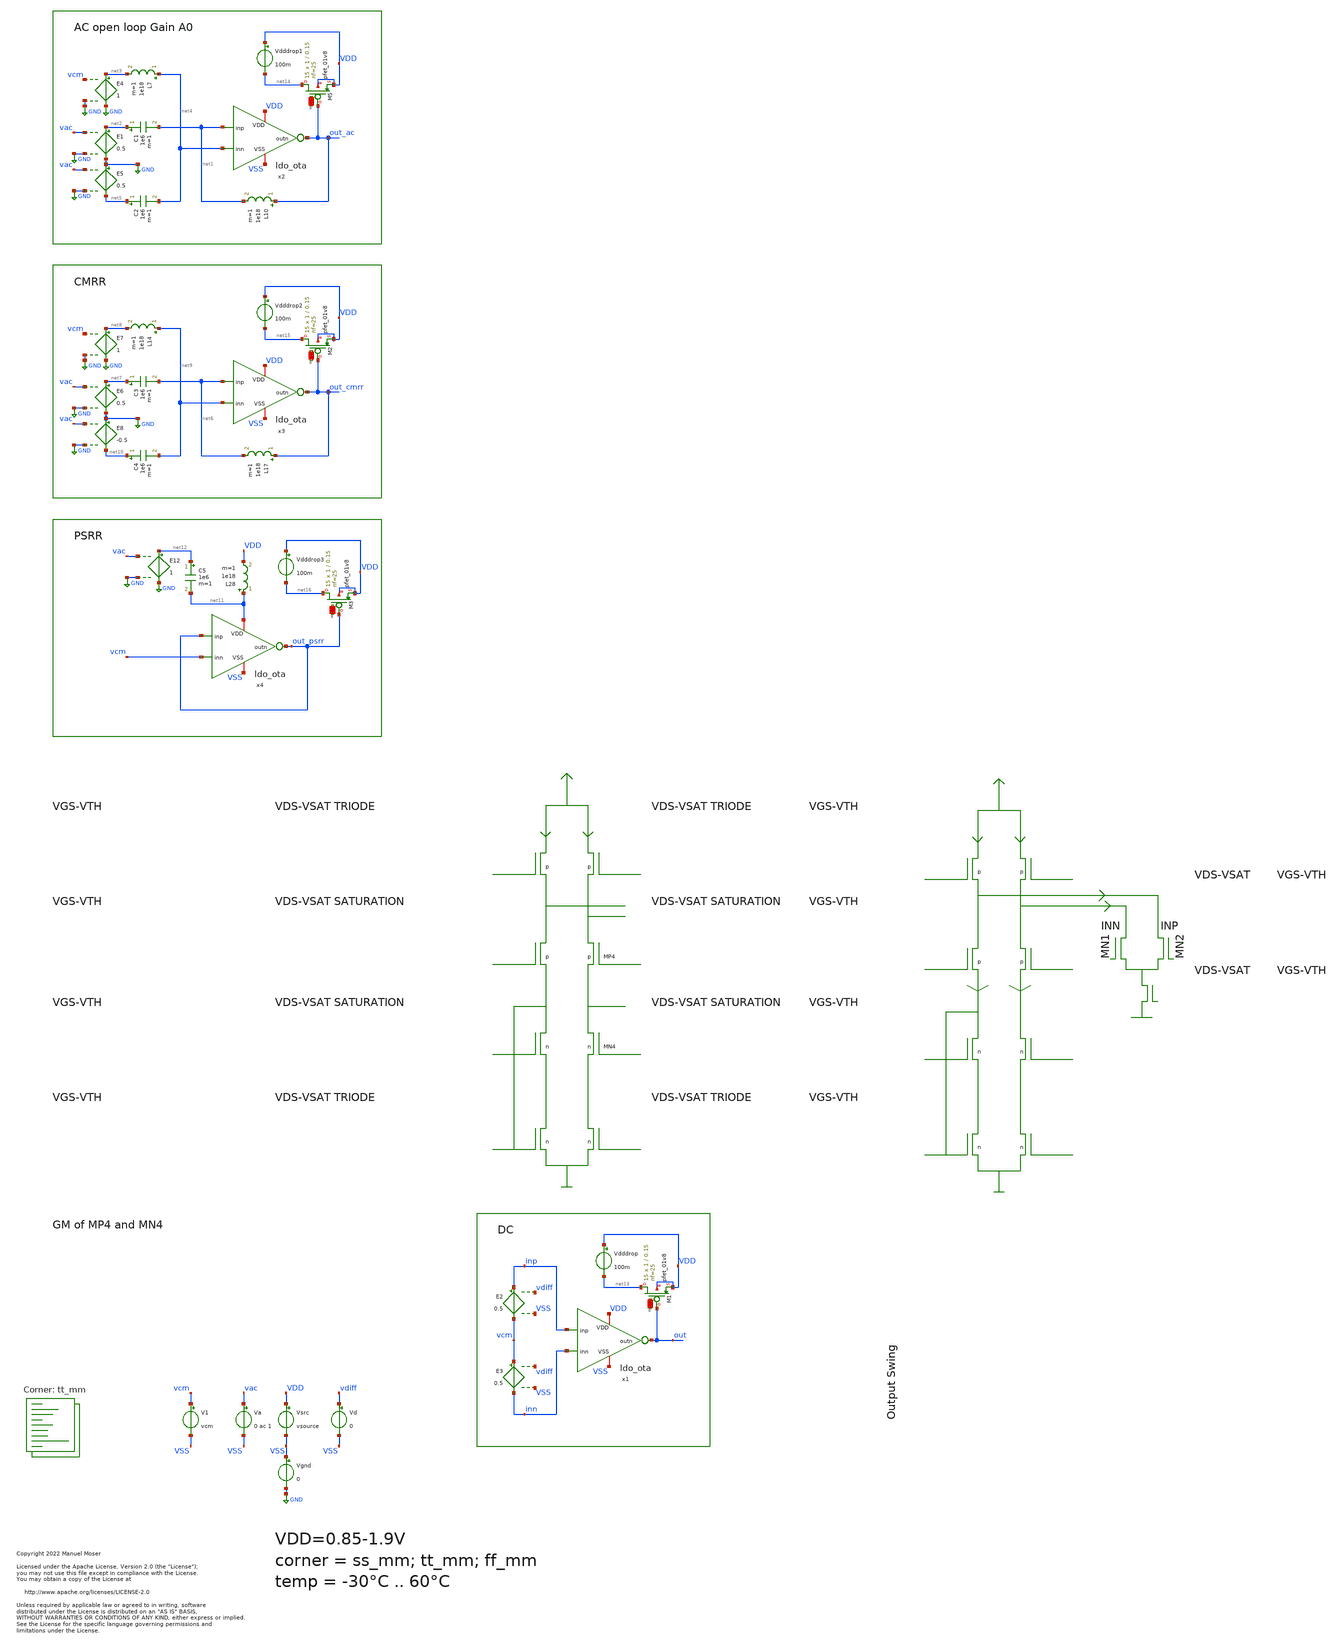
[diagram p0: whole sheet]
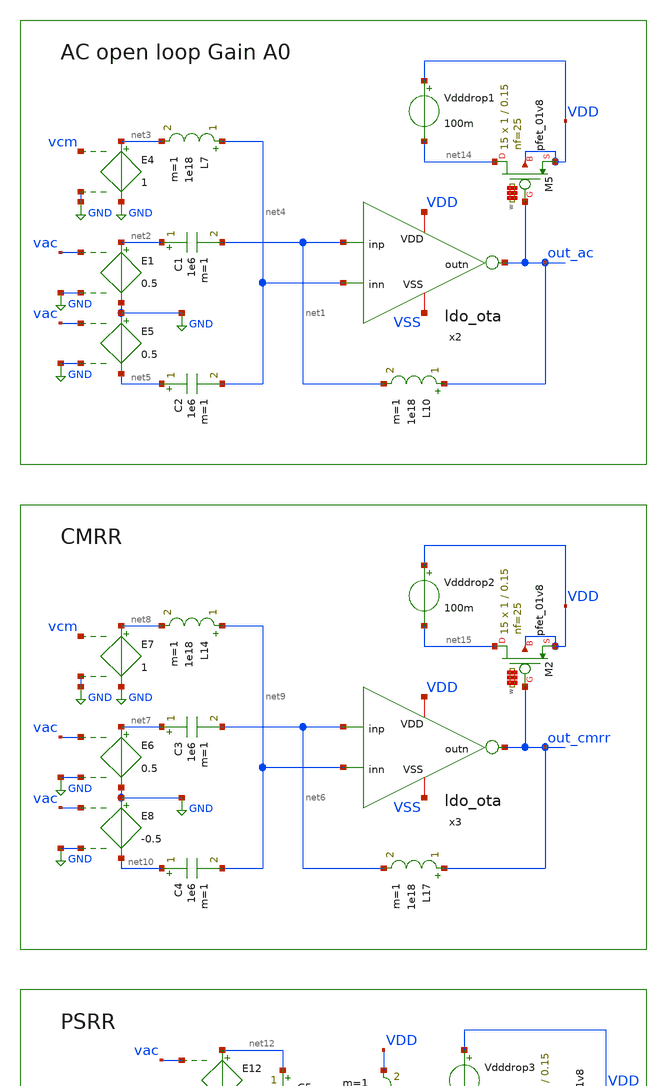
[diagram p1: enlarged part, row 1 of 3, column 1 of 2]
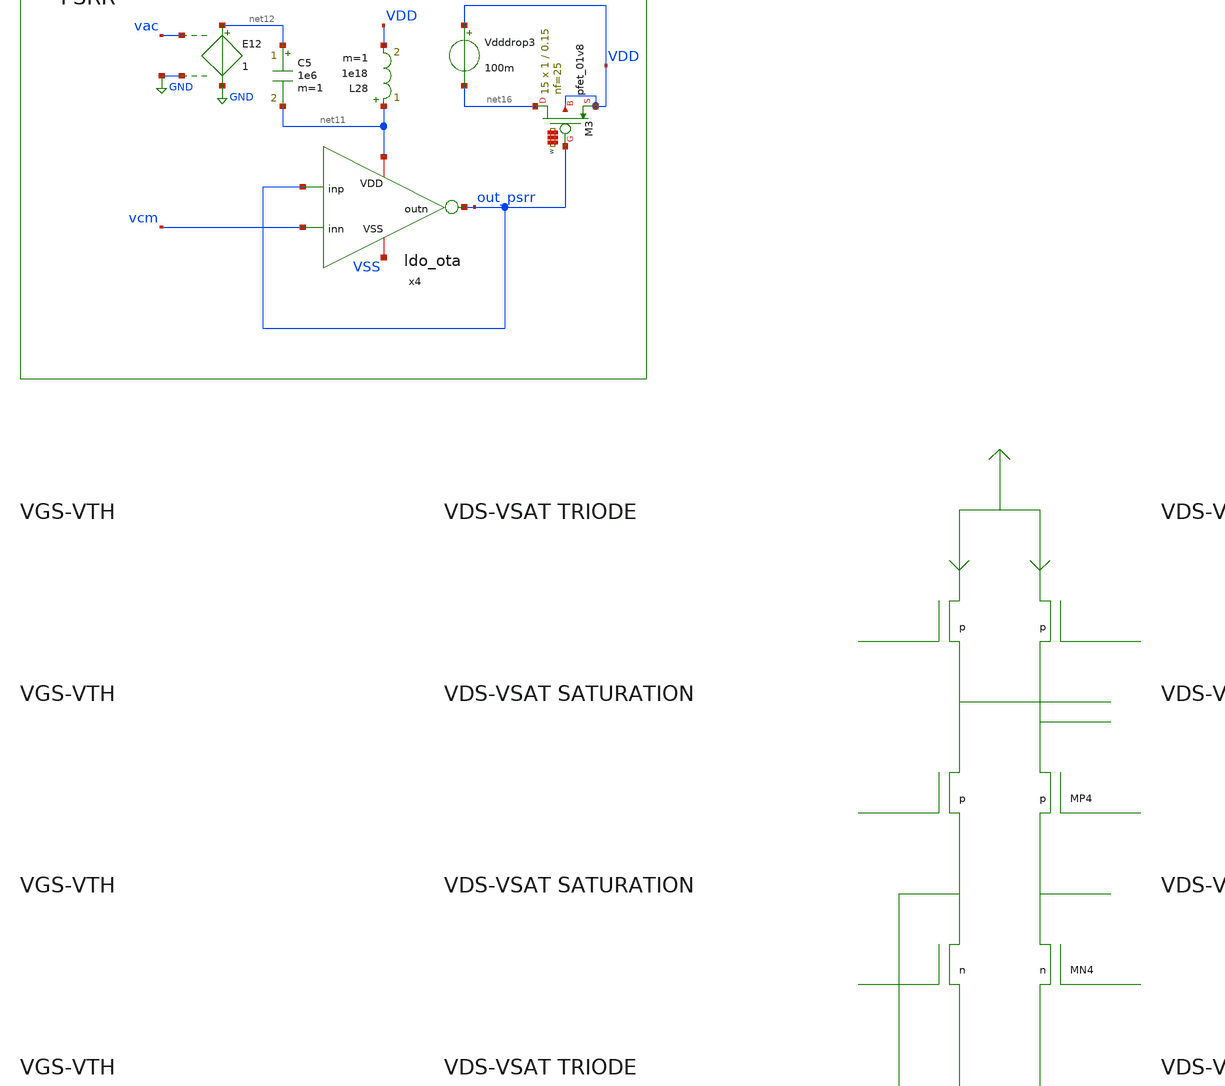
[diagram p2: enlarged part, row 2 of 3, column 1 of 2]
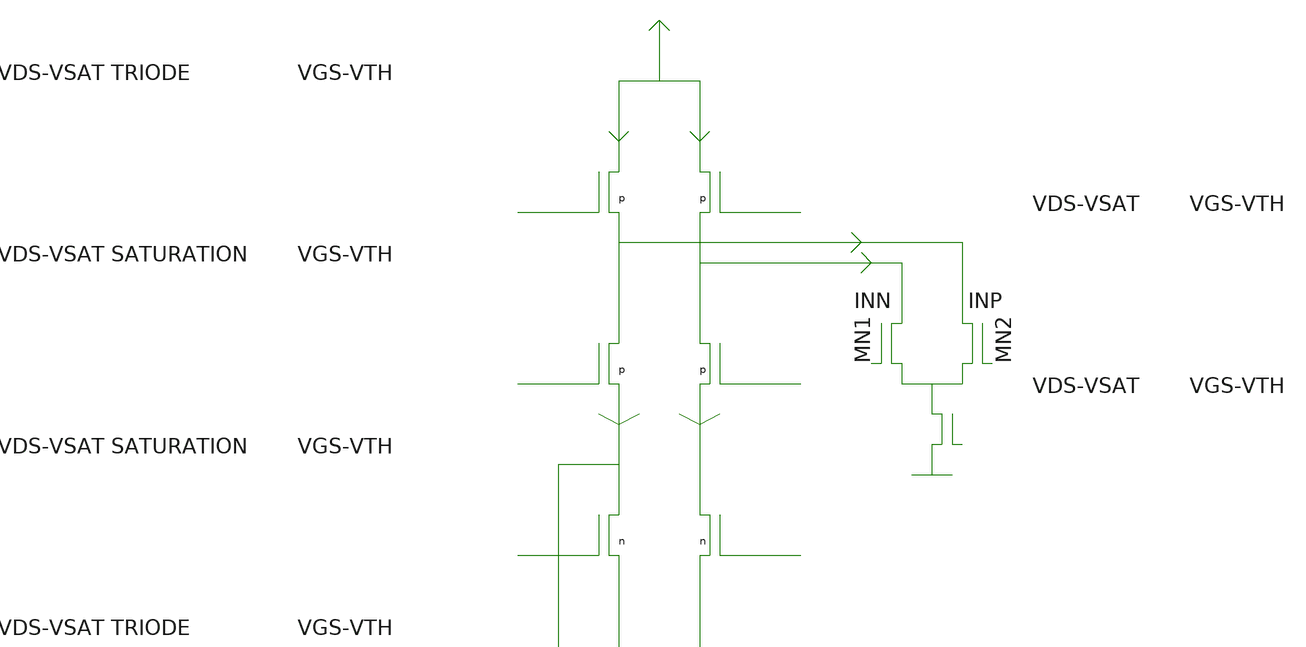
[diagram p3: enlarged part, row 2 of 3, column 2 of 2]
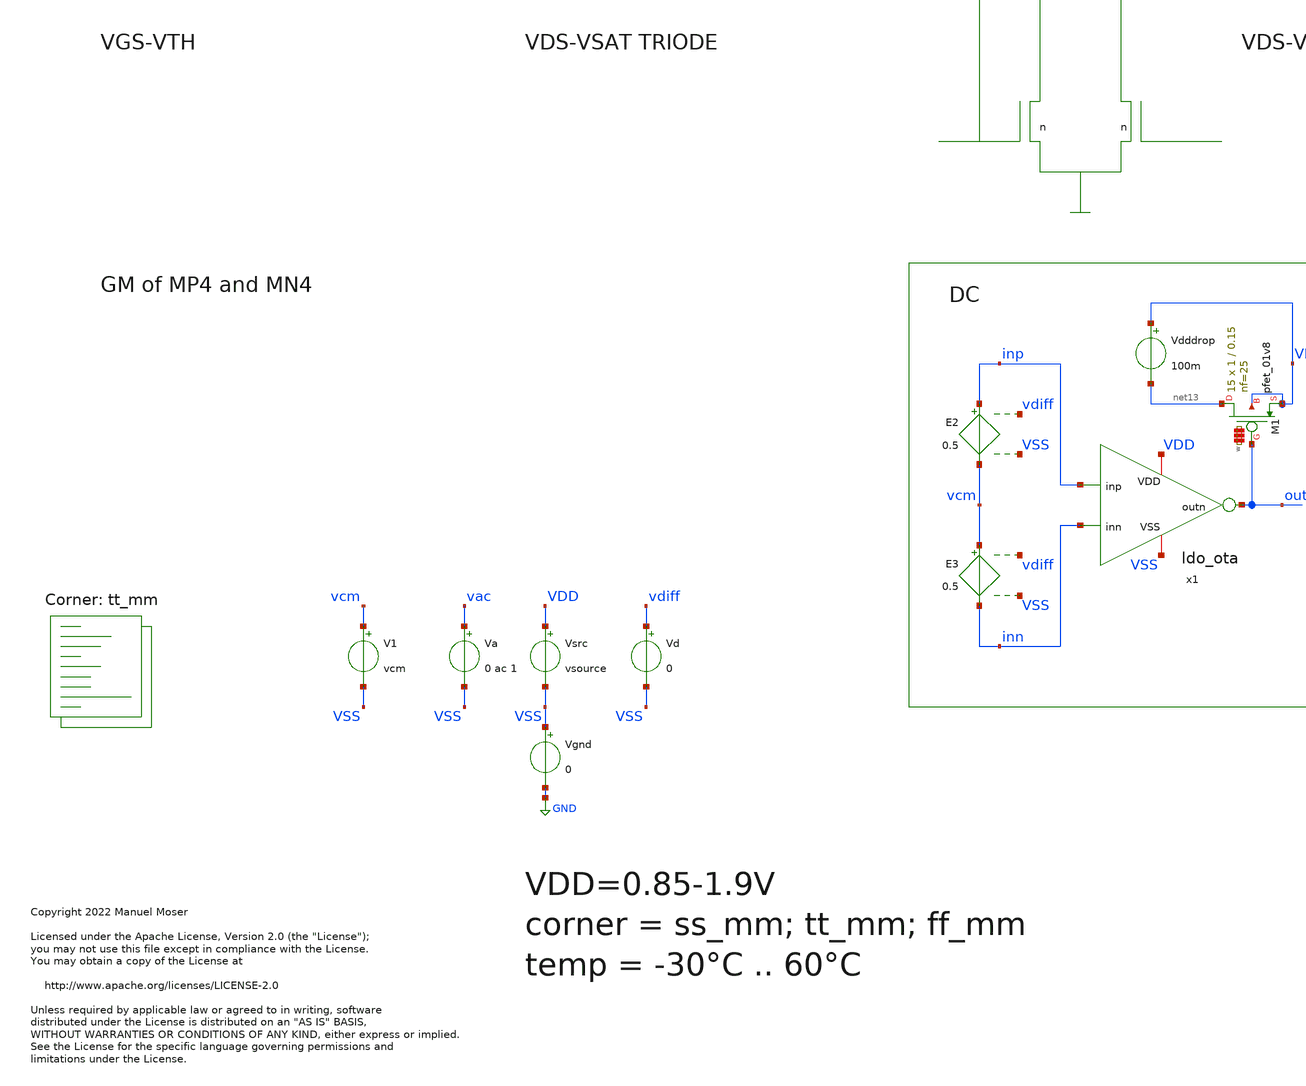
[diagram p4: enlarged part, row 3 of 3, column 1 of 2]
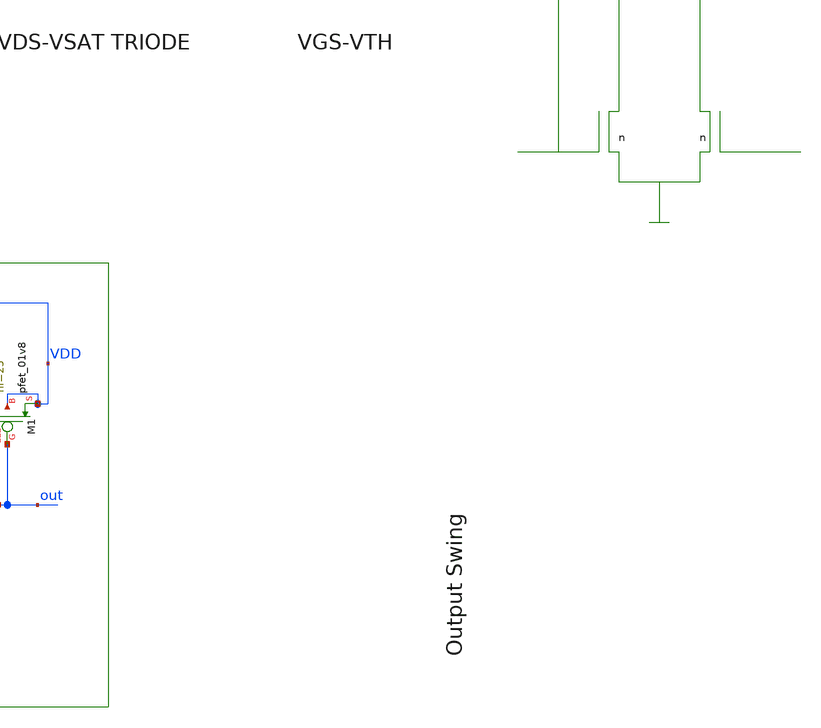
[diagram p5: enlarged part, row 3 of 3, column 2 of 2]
** sch_path: xschem/ldo_ota_tb.sch
* Copyright 2022 Manuel Moser
* Licensed under the Apache License, Version 2.0 (the "License");
**.subckt ldo_ota_tb
V1 vcm VSS vcm
Vd vdiff VSS 0
Vsrc VDD VSS vsource
E2 inp vcm vdiff VSS 0.5
E3 vcm inn vdiff VSS 0.5
Vgnd VSS GND 0
x2 VDD net1 out_ac net4 VSS ldo_ota
Va vac VSS 0 ac 1
E1 net2 GND vac GND 0.5
C1 net2 net1 1e6 m=1
L7 net4 net3 1e18 m=1
E4 net3 GND vcm GND 1
L10 out_ac net1 1e18 m=1
E5 GND net5 vac GND 0.5
C2 net5 net4 1e6 m=1
x3 VDD net6 out_cmrr net9 VSS ldo_ota
E6 net7 GND vac GND 0.5
C3 net7 net6 1e6 m=1
L14 net9 net8 1e18 m=1
E7 net8 GND vcm GND 1
L17 out_cmrr net6 1e18 m=1
E8 GND net10 vac GND -0.5
C4 net10 net9 1e6 m=1
x4 net11 out_psrr out_psrr vcm VSS ldo_ota
C5 net12 net11 1e6 m=1
L28 net11 VDD 1e18 m=1
E12 net12 GND vac GND 1
Vdddrop VDD net13 100m
Vdddrop1 VDD net14 100m
Vdddrop2 VDD net15 100m
Vdddrop3 VDD net16 100m
XM1 net13 out VDD VDD sky130_fd_pr__pfet_01v8 L=0.15 W='1 * 25 ' nf=25 ad='int((nf+1)/2) * W / nf * 0.29'
+ as='int((nf+2)/2) * W / nf * 0.29' pd='2*int((nf+1)/2) * (W / nf + 0.29)' ps='2*int((nf+2)/2) * (W / nf + 0.29)'
+ nrd='0.29 / W ' nrs='0.29 / W ' sa=0 sb=0 sd=0 mult=15 m=15
XM5 net14 out_ac VDD VDD sky130_fd_pr__pfet_01v8 L=0.15 W='1 * 25 ' nf=25 ad='int((nf+1)/2) * W / nf * 0.29'
+ as='int((nf+2)/2) * W / nf * 0.29' pd='2*int((nf+1)/2) * (W / nf + 0.29)' ps='2*int((nf+2)/2) * (W / nf + 0.29)'
+ nrd='0.29 / W ' nrs='0.29 / W ' sa=0 sb=0 sd=0 mult=15 m=15
XM2 net15 out_cmrr VDD VDD sky130_fd_pr__pfet_01v8 L=0.15 W='1 * 25 ' nf=25 ad='int((nf+1)/2) * W / nf * 0.29'
+ as='int((nf+2)/2) * W / nf * 0.29' pd='2*int((nf+1)/2) * (W / nf + 0.29)' ps='2*int((nf+2)/2) * (W / nf + 0.29)'
+ nrd='0.29 / W ' nrs='0.29 / W ' sa=0 sb=0 sd=0 mult=15 m=15
XM3 net16 out_psrr VDD VDD sky130_fd_pr__pfet_01v8 L=0.15 W='1 * 25 ' nf=25 ad='int((nf+1)/2) * W / nf * 0.29'
+ as='int((nf+2)/2) * W / nf * 0.29' pd='2*int((nf+1)/2) * (W / nf + 0.29)' ps='2*int((nf+2)/2) * (W / nf + 0.29)'
+ nrd='0.29 / W ' nrs='0.29 / W ' sa=0 sb=0 sd=0 mult=15 m=15
x1 VDD inp out inn VSS ldo_ota
**** begin user architecture code



.temp 27
*.options savecurrents
.option gmin = 1e-16
.option RSHUNT=1E20

.param vsource = 1.8
.param vcm = {vsource/2}


.save all
 + @m.x1.x1.xmn1.msky130_fd_pr__nfet_01v8_lvt[vgs] @m.x1.x1.xmn1.msky130_fd_pr__nfet_01v8_lvt[vth]
+ @m.x1.x1.xmn1.msky130_fd_pr__nfet_01v8_lvt[vds] @m.x1.x1.xmn1.msky130_fd_pr__nfet_01v8_lvt[vdsat] @m.x1.x1.xmn1.msky130_fd_pr__nfet_01v8_lvt[id]
+ @m.x1.x1.xmn1.msky130_fd_pr__nfet_01v8_lvt[gm]
 + @m.x1.x1.xmn2.msky130_fd_pr__nfet_01v8_lvt[vgs] @m.x1.x1.xmn2.msky130_fd_pr__nfet_01v8_lvt[vth]
+ @m.x1.x1.xmn2.msky130_fd_pr__nfet_01v8_lvt[vds] @m.x1.x1.xmn2.msky130_fd_pr__nfet_01v8_lvt[vdsat] @m.x1.x1.xmn2.msky130_fd_pr__nfet_01v8_lvt[id]
+ @m.x1.x1.xmn2.msky130_fd_pr__nfet_01v8_lvt[gm]
 + @m.x1.x1.xmn3.msky130_fd_pr__nfet_01v8_lvt[vgs] @m.x1.x1.xmn3.msky130_fd_pr__nfet_01v8_lvt[vth]
+ @m.x1.x1.xmn3.msky130_fd_pr__nfet_01v8_lvt[vds] @m.x1.x1.xmn3.msky130_fd_pr__nfet_01v8_lvt[vdsat] @m.x1.x1.xmn3.msky130_fd_pr__nfet_01v8_lvt[id]
+ @m.x1.x1.xmn3.msky130_fd_pr__nfet_01v8_lvt[gm]
 + @m.x1.x1.xmn4.msky130_fd_pr__nfet_01v8_lvt[vgs] @m.x1.x1.xmn4.msky130_fd_pr__nfet_01v8_lvt[vth]
+ @m.x1.x1.xmn4.msky130_fd_pr__nfet_01v8_lvt[vds] @m.x1.x1.xmn4.msky130_fd_pr__nfet_01v8_lvt[vdsat] @m.x1.x1.xmn4.msky130_fd_pr__nfet_01v8_lvt[id]
+ @m.x1.x1.xmn4.msky130_fd_pr__nfet_01v8_lvt[gm]
 + @m.x1.x1.xmn5.msky130_fd_pr__nfet_01v8_lvt[vgs] @m.x1.x1.xmn5.msky130_fd_pr__nfet_01v8_lvt[vth]
+ @m.x1.x1.xmn5.msky130_fd_pr__nfet_01v8_lvt[vds] @m.x1.x1.xmn5.msky130_fd_pr__nfet_01v8_lvt[vdsat] @m.x1.x1.xmn5.msky130_fd_pr__nfet_01v8_lvt[id]
+ @m.x1.x1.xmn5.msky130_fd_pr__nfet_01v8_lvt[gm]
 + @m.x1.x1.xmn6.msky130_fd_pr__nfet_01v8_lvt[vgs] @m.x1.x1.xmn6.msky130_fd_pr__nfet_01v8_lvt[vth]
+ @m.x1.x1.xmn6.msky130_fd_pr__nfet_01v8_lvt[vds] @m.x1.x1.xmn6.msky130_fd_pr__nfet_01v8_lvt[vdsat] @m.x1.x1.xmn6.msky130_fd_pr__nfet_01v8_lvt[id]
+ @m.x1.x1.xmn6.msky130_fd_pr__nfet_01v8_lvt[gm]
 + @m.x1.x1.xmn7.msky130_fd_pr__nfet_01v8_lvt[vgs] @m.x1.x1.xmn7.msky130_fd_pr__nfet_01v8_lvt[vth]
+ @m.x1.x1.xmn7.msky130_fd_pr__nfet_01v8_lvt[vds] @m.x1.x1.xmn7.msky130_fd_pr__nfet_01v8_lvt[vdsat] @m.x1.x1.xmn7.msky130_fd_pr__nfet_01v8_lvt[id]
+ @m.x1.x1.xmn7.msky130_fd_pr__nfet_01v8_lvt[gm]
 + @m.x1.x1.xmp1.msky130_fd_pr__pfet_01v8_lvt[vgs] @m.x1.x1.xmp1.msky130_fd_pr__pfet_01v8_lvt[vth]
+ @m.x1.x1.xmp1.msky130_fd_pr__pfet_01v8_lvt[vds] @m.x1.x1.xmp1.msky130_fd_pr__pfet_01v8_lvt[vdsat] @m.x1.x1.xmp1.msky130_fd_pr__pfet_01v8_lvt[id]
+ @m.x1.x1.xmp1.msky130_fd_pr__pfet_01v8_lvt[gm]
 + @m.x1.x1.xmp2.msky130_fd_pr__pfet_01v8_lvt[vgs] @m.x1.x1.xmp2.msky130_fd_pr__pfet_01v8_lvt[vth]
+ @m.x1.x1.xmp2.msky130_fd_pr__pfet_01v8_lvt[vds] @m.x1.x1.xmp2.msky130_fd_pr__pfet_01v8_lvt[vdsat] @m.x1.x1.xmp2.msky130_fd_pr__pfet_01v8_lvt[id]
+ @m.x1.x1.xmp2.msky130_fd_pr__pfet_01v8_lvt[gm]
 + @m.x1.x1.xmp3.msky130_fd_pr__pfet_01v8_lvt[vgs] @m.x1.x1.xmp3.msky130_fd_pr__pfet_01v8_lvt[vth]
+ @m.x1.x1.xmp3.msky130_fd_pr__pfet_01v8_lvt[vds] @m.x1.x1.xmp3.msky130_fd_pr__pfet_01v8_lvt[vdsat] @m.x1.x1.xmp3.msky130_fd_pr__pfet_01v8_lvt[id]
+ @m.x1.x1.xmp3.msky130_fd_pr__pfet_01v8_lvt[gm]
 + @m.x1.x1.xmp4.msky130_fd_pr__pfet_01v8_lvt[vgs] @m.x1.x1.xmp4.msky130_fd_pr__pfet_01v8_lvt[vth]
+ @m.x1.x1.xmp4.msky130_fd_pr__pfet_01v8_lvt[vds] @m.x1.x1.xmp4.msky130_fd_pr__pfet_01v8_lvt[vdsat] @m.x1.x1.xmp4.msky130_fd_pr__pfet_01v8_lvt[id]
+ @m.x1.x1.xmp4.msky130_fd_pr__pfet_01v8_lvt[gm]

.control
set num_threads = 12
write results.raw
*write results_ac.raw
set appendwrite

repeat 10
 reset
 dc vd -300m 300m 1m temp -30 60 90

write results.raw out x1.bias1 x1.bias2 x1.bias3 x1.bias4
 + @m.x1.x1.xmn1.msky130_fd_pr__nfet_01v8_lvt[vgs] @m.x1.x1.xmn1.msky130_fd_pr__nfet_01v8_lvt[vth]
+ @m.x1.x1.xmn1.msky130_fd_pr__nfet_01v8_lvt[vds] @m.x1.x1.xmn1.msky130_fd_pr__nfet_01v8_lvt[vdsat] @m.x1.x1.xmn1.msky130_fd_pr__nfet_01v8_lvt[id]
+ @m.x1.x1.xmn1.msky130_fd_pr__nfet_01v8_lvt[gm]
 + @m.x1.x1.xmn2.msky130_fd_pr__nfet_01v8_lvt[vgs] @m.x1.x1.xmn2.msky130_fd_pr__nfet_01v8_lvt[vth]
+ @m.x1.x1.xmn2.msky130_fd_pr__nfet_01v8_lvt[vds] @m.x1.x1.xmn2.msky130_fd_pr__nfet_01v8_lvt[vdsat] @m.x1.x1.xmn2.msky130_fd_pr__nfet_01v8_lvt[id]
+ @m.x1.x1.xmn2.msky130_fd_pr__nfet_01v8_lvt[gm]
 + @m.x1.x1.xmn3.msky130_fd_pr__nfet_01v8_lvt[vgs] @m.x1.x1.xmn3.msky130_fd_pr__nfet_01v8_lvt[vth]
+ @m.x1.x1.xmn3.msky130_fd_pr__nfet_01v8_lvt[vds] @m.x1.x1.xmn3.msky130_fd_pr__nfet_01v8_lvt[vdsat] @m.x1.x1.xmn3.msky130_fd_pr__nfet_01v8_lvt[id]
+ @m.x1.x1.xmn3.msky130_fd_pr__nfet_01v8_lvt[gm]
 + @m.x1.x1.xmn4.msky130_fd_pr__nfet_01v8_lvt[vgs] @m.x1.x1.xmn4.msky130_fd_pr__nfet_01v8_lvt[vth]
+ @m.x1.x1.xmn4.msky130_fd_pr__nfet_01v8_lvt[vds] @m.x1.x1.xmn4.msky130_fd_pr__nfet_01v8_lvt[vdsat] @m.x1.x1.xmn4.msky130_fd_pr__nfet_01v8_lvt[id]
+ @m.x1.x1.xmn4.msky130_fd_pr__nfet_01v8_lvt[gm]
 + @m.x1.x1.xmn5.msky130_fd_pr__nfet_01v8_lvt[vgs] @m.x1.x1.xmn5.msky130_fd_pr__nfet_01v8_lvt[vth]
+ @m.x1.x1.xmn5.msky130_fd_pr__nfet_01v8_lvt[vds] @m.x1.x1.xmn5.msky130_fd_pr__nfet_01v8_lvt[vdsat] @m.x1.x1.xmn5.msky130_fd_pr__nfet_01v8_lvt[id]
+ @m.x1.x1.xmn5.msky130_fd_pr__nfet_01v8_lvt[gm]
 + @m.x1.x1.xmn6.msky130_fd_pr__nfet_01v8_lvt[vgs] @m.x1.x1.xmn6.msky130_fd_pr__nfet_01v8_lvt[vth]
+ @m.x1.x1.xmn6.msky130_fd_pr__nfet_01v8_lvt[vds] @m.x1.x1.xmn6.msky130_fd_pr__nfet_01v8_lvt[vdsat] @m.x1.x1.xmn6.msky130_fd_pr__nfet_01v8_lvt[id]
+ @m.x1.x1.xmn6.msky130_fd_pr__nfet_01v8_lvt[gm]
 + @m.x1.x1.xmn7.msky130_fd_pr__nfet_01v8_lvt[vgs] @m.x1.x1.xmn7.msky130_fd_pr__nfet_01v8_lvt[vth]
+ @m.x1.x1.xmn7.msky130_fd_pr__nfet_01v8_lvt[vds] @m.x1.x1.xmn7.msky130_fd_pr__nfet_01v8_lvt[vdsat] @m.x1.x1.xmn7.msky130_fd_pr__nfet_01v8_lvt[id]
+ @m.x1.x1.xmn7.msky130_fd_pr__nfet_01v8_lvt[gm]
 + @m.x1.x1.xmp1.msky130_fd_pr__pfet_01v8_lvt[vgs] @m.x1.x1.xmp1.msky130_fd_pr__pfet_01v8_lvt[vth]
+ @m.x1.x1.xmp1.msky130_fd_pr__pfet_01v8_lvt[vds] @m.x1.x1.xmp1.msky130_fd_pr__pfet_01v8_lvt[vdsat] @m.x1.x1.xmp1.msky130_fd_pr__pfet_01v8_lvt[id]
+ @m.x1.x1.xmp1.msky130_fd_pr__pfet_01v8_lvt[gm]
 + @m.x1.x1.xmp2.msky130_fd_pr__pfet_01v8_lvt[vgs] @m.x1.x1.xmp2.msky130_fd_pr__pfet_01v8_lvt[vth]
+ @m.x1.x1.xmp2.msky130_fd_pr__pfet_01v8_lvt[vds] @m.x1.x1.xmp2.msky130_fd_pr__pfet_01v8_lvt[vdsat] @m.x1.x1.xmp2.msky130_fd_pr__pfet_01v8_lvt[id]
+ @m.x1.x1.xmp2.msky130_fd_pr__pfet_01v8_lvt[gm]
 + @m.x1.x1.xmp3.msky130_fd_pr__pfet_01v8_lvt[vgs] @m.x1.x1.xmp3.msky130_fd_pr__pfet_01v8_lvt[vth]
+ @m.x1.x1.xmp3.msky130_fd_pr__pfet_01v8_lvt[vds] @m.x1.x1.xmp3.msky130_fd_pr__pfet_01v8_lvt[vdsat] @m.x1.x1.xmp3.msky130_fd_pr__pfet_01v8_lvt[id]
+ @m.x1.x1.xmp3.msky130_fd_pr__pfet_01v8_lvt[gm]
 + @m.x1.x1.xmp4.msky130_fd_pr__pfet_01v8_lvt[vgs] @m.x1.x1.xmp4.msky130_fd_pr__pfet_01v8_lvt[vth]
+ @m.x1.x1.xmp4.msky130_fd_pr__pfet_01v8_lvt[vds] @m.x1.x1.xmp4.msky130_fd_pr__pfet_01v8_lvt[vdsat] @m.x1.x1.xmp4.msky130_fd_pr__pfet_01v8_lvt[id]
+ @m.x1.x1.xmp4.msky130_fd_pr__pfet_01v8_lvt[gm]


 ac dec 10 1 10meg
 write results.raw out_ac out_cmrr out_psrr


end

.endc




.lib $::SKYWATER_MODELS/sky130.lib.spice tt_mm
**** end user architecture code
**.ends

* expanding   symbol:  ldo_ota.sym # of pins=5
** sym_path: xschem/ldo_ota.sym
** sch_path: xschem/ldo_ota.sch
.subckt ldo_ota VDD inp outn inn VSS
*.iopin VDD
*.iopin VSS
*.ipin inp
*.ipin inn
*.opin outn
x2 bias2 VDD VSS bias1 ldo_isource
XM10 net1 bias2 VDD VDD sky130_fd_pr__pfet_01v8_lvt L=8 W='1 * 1 ' nf=1 ad='int((nf+1)/2) * W / nf * 0.29'
+ as='int((nf+2)/2) * W / nf * 0.29' pd='2*int((nf+1)/2) * (W / nf + 0.29)' ps='2*int((nf+2)/2) * (W / nf + 0.29)'
+ nrd='0.29 / W ' nrs='0.29 / W ' sa=0 sb=0 sd=0 mult=1 m=1
XM12 bias2 bias2 net1 VDD sky130_fd_pr__pfet_01v8_lvt L=1 W='3 * 9 ' nf=9 ad='int((nf+1)/2) * W / nf * 0.29'
+ as='int((nf+2)/2) * W / nf * 0.29' pd='2*int((nf+1)/2) * (W / nf + 0.29)' ps='2*int((nf+2)/2) * (W / nf + 0.29)'
+ nrd='0.29 / W ' nrs='0.29 / W ' sa=0 sb=0 sd=0 mult=1 m=1
XM1 net2 bias1 VDD VDD sky130_fd_pr__pfet_01v8_lvt L=8 W='1 * 3 ' nf=3 ad='int((nf+1)/2) * W / nf * 0.29'
+ as='int((nf+2)/2) * W / nf * 0.29' pd='2*int((nf+1)/2) * (W / nf + 0.29)' ps='2*int((nf+2)/2) * (W / nf + 0.29)'
+ nrd='0.29 / W ' nrs='0.29 / W ' sa=0 sb=0 sd=0 mult=1 m=1
XM2 bias1 bias2 net2 VDD sky130_fd_pr__pfet_01v8_lvt L=1 W='3 * 9 ' nf=9 ad='int((nf+1)/2) * W / nf * 0.29'
+ as='int((nf+2)/2) * W / nf * 0.29' pd='2*int((nf+1)/2) * (W / nf + 0.29)' ps='2*int((nf+2)/2) * (W / nf + 0.29)'
+ nrd='0.29 / W ' nrs='0.29 / W ' sa=0 sb=0 sd=0 mult=1 m=1
XM3 net3 bias1 VDD VDD sky130_fd_pr__pfet_01v8_lvt L=8 W='1 * 3 ' nf=3 ad='int((nf+1)/2) * W / nf * 0.29'
+ as='int((nf+2)/2) * W / nf * 0.29' pd='2*int((nf+1)/2) * (W / nf + 0.29)' ps='2*int((nf+2)/2) * (W / nf + 0.29)'
+ nrd='0.29 / W ' nrs='0.29 / W ' sa=0 sb=0 sd=0 mult=1 m=1
XM4 bias3 bias2 net3 VDD sky130_fd_pr__pfet_01v8_lvt L=1 W='3 * 9 ' nf=9 ad='int((nf+1)/2) * W / nf * 0.29'
+ as='int((nf+2)/2) * W / nf * 0.29' pd='2*int((nf+1)/2) * (W / nf + 0.29)' ps='2*int((nf+2)/2) * (W / nf + 0.29)'
+ nrd='0.29 / W ' nrs='0.29 / W ' sa=0 sb=0 sd=0 mult=1 m=1
XM5 net4 bias1 VDD VDD sky130_fd_pr__pfet_01v8_lvt L=8 W='1 * 3 ' nf=3 ad='int((nf+1)/2) * W / nf * 0.29'
+ as='int((nf+2)/2) * W / nf * 0.29' pd='2*int((nf+1)/2) * (W / nf + 0.29)' ps='2*int((nf+2)/2) * (W / nf + 0.29)'
+ nrd='0.29 / W ' nrs='0.29 / W ' sa=0 sb=0 sd=0 mult=1 m=1
XM8 bias4 bias2 net4 VDD sky130_fd_pr__pfet_01v8_lvt L=1 W='3 * 9 ' nf=9 ad='int((nf+1)/2) * W / nf * 0.29'
+ as='int((nf+2)/2) * W / nf * 0.29' pd='2*int((nf+1)/2) * (W / nf + 0.29)' ps='2*int((nf+2)/2) * (W / nf + 0.29)'
+ nrd='0.29 / W ' nrs='0.29 / W ' sa=0 sb=0 sd=0 mult=1 m=1
XM9 bias3 bias3 net5 VSS sky130_fd_pr__nfet_01v8_lvt L=4 W='1 * 9 ' nf=9 ad='int((nf+1)/2) * W / nf * 0.29'
+ as='int((nf+2)/2) * W / nf * 0.29' pd='2*int((nf+1)/2) * (W / nf + 0.29)' ps='2*int((nf+2)/2) * (W / nf + 0.29)'
+ nrd='0.29 / W ' nrs='0.29 / W ' sa=0 sb=0 sd=0 mult=1 m=1
XM11 net5 bias3 net10 VSS sky130_fd_pr__nfet_01v8_lvt L=4 W='1 * 1 ' nf=1 ad='int((nf+1)/2) * W / nf * 0.29'
+ as='int((nf+2)/2) * W / nf * 0.29' pd='2*int((nf+1)/2) * (W / nf + 0.29)' ps='2*int((nf+2)/2) * (W / nf + 0.29)'
+ nrd='0.29 / W ' nrs='0.29 / W ' sa=0 sb=0 sd=0 mult=1 m=1
XM13 bias4 bias3 net6 VSS sky130_fd_pr__nfet_01v8_lvt L=4 W='1 * 9 ' nf=9 ad='int((nf+1)/2) * W / nf * 0.29'
+ as='int((nf+2)/2) * W / nf * 0.29' pd='2*int((nf+1)/2) * (W / nf + 0.29)' ps='2*int((nf+2)/2) * (W / nf + 0.29)'
+ nrd='0.29 / W ' nrs='0.29 / W ' sa=0 sb=0 sd=0 mult=1 m=1
XM14 net6 bias4 net7 VSS sky130_fd_pr__nfet_01v8_lvt L=4 W='1 * 3 ' nf=3 ad='int((nf+1)/2) * W / nf * 0.29'
+ as='int((nf+2)/2) * W / nf * 0.29' pd='2*int((nf+1)/2) * (W / nf + 0.29)' ps='2*int((nf+2)/2) * (W / nf + 0.29)'
+ nrd='0.29 / W ' nrs='0.29 / W ' sa=0 sb=0 sd=0 mult=1 m=1
XM6 net7 bias4 net8 VSS sky130_fd_pr__nfet_01v8_lvt L=4 W='1 * 3 ' nf=3 ad='int((nf+1)/2) * W / nf * 0.29'
+ as='int((nf+2)/2) * W / nf * 0.29' pd='2*int((nf+1)/2) * (W / nf + 0.29)' ps='2*int((nf+2)/2) * (W / nf + 0.29)'
+ nrd='0.29 / W ' nrs='0.29 / W ' sa=0 sb=0 sd=0 mult=1 m=1
XM7 net10 bias3 net9 VSS sky130_fd_pr__nfet_01v8_lvt L=4 W='1 * 1 ' nf=1 ad='int((nf+1)/2) * W / nf * 0.29'
+ as='int((nf+2)/2) * W / nf * 0.29' pd='2*int((nf+1)/2) * (W / nf + 0.29)' ps='2*int((nf+2)/2) * (W / nf + 0.29)'
+ nrd='0.29 / W ' nrs='0.29 / W ' sa=0 sb=0 sd=0 mult=1 m=1
XM15 net8 bias4 VSS VSS sky130_fd_pr__nfet_01v8_lvt L=4 W='1 * 3 ' nf=3 ad='int((nf+1)/2) * W / nf * 0.29'
+ as='int((nf+2)/2) * W / nf * 0.29' pd='2*int((nf+1)/2) * (W / nf + 0.29)' ps='2*int((nf+2)/2) * (W / nf + 0.29)'
+ nrd='0.29 / W ' nrs='0.29 / W ' sa=0 sb=0 sd=0 mult=1 m=1
XM16 net9 bias3 VSS VSS sky130_fd_pr__nfet_01v8_lvt L=4 W='1 * 1 ' nf=1 ad='int((nf+1)/2) * W / nf * 0.29'
+ as='int((nf+2)/2) * W / nf * 0.29' pd='2*int((nf+1)/2) * (W / nf + 0.29)' ps='2*int((nf+2)/2) * (W / nf + 0.29)'
+ nrd='0.29 / W ' nrs='0.29 / W ' sa=0 sb=0 sd=0 mult=1 m=1
x1 VDD inp inn bias1 bias2 bias3 outn VSS bias4 ldo_fc_n
.ends


* expanding   symbol:  ldo_isource.sym # of pins=4
** sym_path: xschem/ldo_isource.sym
** sch_path: xschem/ldo_isource.sch
.subckt ldo_isource curr_n1 VDD VSS curr_n2
*.iopin VDD
*.iopin VSS
*.ipin curr_n1
*.ipin curr_n2
XMP2 VGP VGP net4 VDD sky130_fd_pr__pfet_01v8_lvt L=8 W='0.55 * 7 ' nf=7 ad='int((nf+1)/2) * W / nf * 0.29'
+ as='int((nf+2)/2) * W / nf * 0.29' pd='2*int((nf+1)/2) * (W / nf + 0.29)' ps='2*int((nf+2)/2) * (W / nf + 0.29)'
+ nrd='0.29 / W ' nrs='0.29 / W ' sa=0 sb=0 sd=0 mult=1 m=1
XMP1 VGN VGP net3 VDD sky130_fd_pr__pfet_01v8_lvt L=8 W='0.55 * 7 ' nf=7 ad='int((nf+1)/2) * W / nf * 0.29'
+ as='int((nf+2)/2) * W / nf * 0.29' pd='2*int((nf+1)/2) * (W / nf + 0.29)' ps='2*int((nf+2)/2) * (W / nf + 0.29)'
+ nrd='0.29 / W ' nrs='0.29 / W ' sa=0 sb=0 sd=0 mult=1 m=1
XMN1 VGN VGN net1 VSS sky130_fd_pr__nfet_01v8_lvt L=8 W='7 * 1 ' nf=1 ad='int((nf+1)/2) * W / nf * 0.29'
+ as='int((nf+2)/2) * W / nf * 0.29' pd='2*int((nf+1)/2) * (W / nf + 0.29)' ps='2*int((nf+2)/2) * (W / nf + 0.29)'
+ nrd='0.29 / W ' nrs='0.29 / W ' sa=0 sb=0 sd=0 mult=1 m=1
XMN2 VGP VGN net2 VSS sky130_fd_pr__nfet_01v8_lvt L=8 W='7 * 1 ' nf=1 ad='int((nf+1)/2) * W / nf * 0.29'
+ as='int((nf+2)/2) * W / nf * 0.29' pd='2*int((nf+1)/2) * (W / nf + 0.29)' ps='2*int((nf+2)/2) * (W / nf + 0.29)'
+ nrd='0.29 / W ' nrs='0.29 / W ' sa=0 sb=0 sd=0 mult=5 m=5
XMN3 net1 VGN VSS VSS sky130_fd_pr__nfet_01v8_lvt L=8 W='7 * 1 ' nf=1 ad='int((nf+1)/2) * W / nf * 0.29'
+ as='int((nf+2)/2) * W / nf * 0.29' pd='2*int((nf+1)/2) * (W / nf + 0.29)' ps='2*int((nf+2)/2) * (W / nf + 0.29)'
+ nrd='0.29 / W ' nrs='0.29 / W ' sa=0 sb=0 sd=0 mult=1 m=1
XMN4 net2 VGN Vref VSS sky130_fd_pr__nfet_01v8_lvt L=8 W='7 * 1 ' nf=1 ad='int((nf+1)/2) * W / nf * 0.29'
+ as='int((nf+2)/2) * W / nf * 0.29' pd='2*int((nf+1)/2) * (W / nf + 0.29)' ps='2*int((nf+2)/2) * (W / nf + 0.29)'
+ nrd='0.29 / W ' nrs='0.29 / W ' sa=0 sb=0 sd=0 mult=5 m=5
XMP4 net3 VGP VDD VDD sky130_fd_pr__pfet_01v8_lvt L=8 W='0.55 * 7 ' nf=7 ad='int((nf+1)/2) * W / nf * 0.29'
+ as='int((nf+2)/2) * W / nf * 0.29' pd='2*int((nf+1)/2) * (W / nf + 0.29)' ps='2*int((nf+2)/2) * (W / nf + 0.29)'
+ nrd='0.29 / W ' nrs='0.29 / W ' sa=0 sb=0 sd=0 mult=1 m=1
XMP5 net4 VGP VDD VDD sky130_fd_pr__pfet_01v8_lvt L=8 W='0.55 * 7 ' nf=7 ad='int((nf+1)/2) * W / nf * 0.29'
+ as='int((nf+2)/2) * W / nf * 0.29' pd='2*int((nf+1)/2) * (W / nf + 0.29)' ps='2*int((nf+2)/2) * (W / nf + 0.29)'
+ nrd='0.29 / W ' nrs='0.29 / W ' sa=0 sb=0 sd=0 mult=1 m=1
XMP3 Vrefgate VGP net19 VDD sky130_fd_pr__pfet_01v8_lvt L=8 W='0.55 * 7 ' nf=7 ad='int((nf+1)/2) * W / nf * 0.29'
+ as='int((nf+2)/2) * W / nf * 0.29' pd='2*int((nf+1)/2) * (W / nf + 0.29)' ps='2*int((nf+2)/2) * (W / nf + 0.29)'
+ nrd='0.29 / W ' nrs='0.29 / W ' sa=0 sb=0 sd=0 mult=1 m=1
XM2 net5 Vrefgate net6 VSS sky130_fd_pr__nfet_01v8 L=4 W='1 * 1 ' nf=1 ad='int((nf+1)/2) * W / nf * 0.29'
+ as='int((nf+2)/2) * W / nf * 0.29' pd='2*int((nf+1)/2) * (W / nf + 0.29)' ps='2*int((nf+2)/2) * (W / nf + 0.29)'
+ nrd='0.29 / W ' nrs='0.29 / W ' sa=0 sb=0 sd=0 mult=1 m=1
XM3 net8 Vrefgate VSS VSS sky130_fd_pr__nfet_01v8 L=4 W='1 * 1 ' nf=1 ad='int((nf+1)/2) * W / nf * 0.29'
+ as='int((nf+2)/2) * W / nf * 0.29' pd='2*int((nf+1)/2) * (W / nf + 0.29)' ps='2*int((nf+2)/2) * (W / nf + 0.29)'
+ nrd='0.29 / W ' nrs='0.29 / W ' sa=0 sb=0 sd=0 mult=1 m=1
XM1 net7 Vrefgate net8 VSS sky130_fd_pr__nfet_01v8 L=4 W='1 * 1 ' nf=1 ad='int((nf+1)/2) * W / nf * 0.29'
+ as='int((nf+2)/2) * W / nf * 0.29' pd='2*int((nf+1)/2) * (W / nf + 0.29)' ps='2*int((nf+2)/2) * (W / nf + 0.29)'
+ nrd='0.29 / W ' nrs='0.29 / W ' sa=0 sb=0 sd=0 mult=1 m=1
XM4 net6 Vrefgate net7 VSS sky130_fd_pr__nfet_01v8 L=4 W='1 * 1 ' nf=1 ad='int((nf+1)/2) * W / nf * 0.29'
+ as='int((nf+2)/2) * W / nf * 0.29' pd='2*int((nf+1)/2) * (W / nf + 0.29)' ps='2*int((nf+2)/2) * (W / nf + 0.29)'
+ nrd='0.29 / W ' nrs='0.29 / W ' sa=0 sb=0 sd=0 mult=1 m=1
XMN5 net10 Vrefgate VSS VSS sky130_fd_pr__nfet_01v8_lvt L=4 W='1 * 1 ' nf=1 ad='int((nf+1)/2) * W / nf * 0.29'
+ as='int((nf+2)/2) * W / nf * 0.29' pd='2*int((nf+1)/2) * (W / nf + 0.29)' ps='2*int((nf+2)/2) * (W / nf + 0.29)'
+ nrd='0.29 / W ' nrs='0.29 / W ' sa=0 sb=0 sd=0 mult=1 m=1
XMN6 net14 Vrefgate net9 VSS sky130_fd_pr__nfet_01v8_lvt L=4 W='1 * 1 ' nf=1 ad='int((nf+1)/2) * W / nf * 0.29'
+ as='int((nf+2)/2) * W / nf * 0.29' pd='2*int((nf+1)/2) * (W / nf + 0.29)' ps='2*int((nf+2)/2) * (W / nf + 0.29)'
+ nrd='0.29 / W ' nrs='0.29 / W ' sa=0 sb=0 sd=0 mult=1 m=1
XMN9 net16 Vrefgate net14 VSS sky130_fd_pr__nfet_01v8_lvt L=4 W='1 * 1 ' nf=1 ad='int((nf+1)/2) * W / nf * 0.29'
+ as='int((nf+2)/2) * W / nf * 0.29' pd='2*int((nf+1)/2) * (W / nf + 0.29)' ps='2*int((nf+2)/2) * (W / nf + 0.29)'
+ nrd='0.29 / W ' nrs='0.29 / W ' sa=0 sb=0 sd=0 mult=1 m=1
XM5 Vrefgate Vrefgate net5 VSS sky130_fd_pr__nfet_01v8 L=4 W='1 * 1 ' nf=1 ad='int((nf+1)/2) * W / nf * 0.29'
+ as='int((nf+2)/2) * W / nf * 0.29' pd='2*int((nf+1)/2) * (W / nf + 0.29)' ps='2*int((nf+2)/2) * (W / nf + 0.29)'
+ nrd='0.29 / W ' nrs='0.29 / W ' sa=0 sb=0 sd=0 mult=1 m=1
XMN10 net11 Vrefgate net10 VSS sky130_fd_pr__nfet_01v8_lvt L=4 W='1 * 1 ' nf=1 ad='int((nf+1)/2) * W / nf * 0.29'
+ as='int((nf+2)/2) * W / nf * 0.29' pd='2*int((nf+1)/2) * (W / nf + 0.29)' ps='2*int((nf+2)/2) * (W / nf + 0.29)'
+ nrd='0.29 / W ' nrs='0.29 / W ' sa=0 sb=0 sd=0 mult=1 m=1
XMN11 net12 Vrefgate net11 VSS sky130_fd_pr__nfet_01v8_lvt L=4 W='1 * 1 ' nf=1 ad='int((nf+1)/2) * W / nf * 0.29'
+ as='int((nf+2)/2) * W / nf * 0.29' pd='2*int((nf+1)/2) * (W / nf + 0.29)' ps='2*int((nf+2)/2) * (W / nf + 0.29)'
+ nrd='0.29 / W ' nrs='0.29 / W ' sa=0 sb=0 sd=0 mult=1 m=1
XMN12 net13 Vrefgate net12 VSS sky130_fd_pr__nfet_01v8_lvt L=4 W='1 * 1 ' nf=1 ad='int((nf+1)/2) * W / nf * 0.29'
+ as='int((nf+2)/2) * W / nf * 0.29' pd='2*int((nf+1)/2) * (W / nf + 0.29)' ps='2*int((nf+2)/2) * (W / nf + 0.29)'
+ nrd='0.29 / W ' nrs='0.29 / W ' sa=0 sb=0 sd=0 mult=1 m=1
XMN13 net9 Vrefgate net13 VSS sky130_fd_pr__nfet_01v8_lvt L=4 W='1 * 1 ' nf=1 ad='int((nf+1)/2) * W / nf * 0.29'
+ as='int((nf+2)/2) * W / nf * 0.29' pd='2*int((nf+1)/2) * (W / nf + 0.29)' ps='2*int((nf+2)/2) * (W / nf + 0.29)'
+ nrd='0.29 / W ' nrs='0.29 / W ' sa=0 sb=0 sd=0 mult=1 m=1
XMN7 net18 Vrefgate net15 VSS sky130_fd_pr__nfet_01v8_lvt L=4 W='1 * 1 ' nf=1 ad='int((nf+1)/2) * W / nf * 0.29'
+ as='int((nf+2)/2) * W / nf * 0.29' pd='2*int((nf+1)/2) * (W / nf + 0.29)' ps='2*int((nf+2)/2) * (W / nf + 0.29)'
+ nrd='0.29 / W ' nrs='0.29 / W ' sa=0 sb=0 sd=0 mult=1 m=1
XMN8 Vref Vrefgate net18 VSS sky130_fd_pr__nfet_01v8_lvt L=4 W='1 * 1 ' nf=1 ad='int((nf+1)/2) * W / nf * 0.29'
+ as='int((nf+2)/2) * W / nf * 0.29' pd='2*int((nf+1)/2) * (W / nf + 0.29)' ps='2*int((nf+2)/2) * (W / nf + 0.29)'
+ nrd='0.29 / W ' nrs='0.29 / W ' sa=0 sb=0 sd=0 mult=1 m=1
XMN14 net17 Vrefgate net16 VSS sky130_fd_pr__nfet_01v8_lvt L=4 W='1 * 1 ' nf=1 ad='int((nf+1)/2) * W / nf * 0.29'
+ as='int((nf+2)/2) * W / nf * 0.29' pd='2*int((nf+1)/2) * (W / nf + 0.29)' ps='2*int((nf+2)/2) * (W / nf + 0.29)'
+ nrd='0.29 / W ' nrs='0.29 / W ' sa=0 sb=0 sd=0 mult=1 m=1
XMN15 net15 Vrefgate net17 VSS sky130_fd_pr__nfet_01v8_lvt L=4 W='1 * 1 ' nf=1 ad='int((nf+1)/2) * W / nf * 0.29'
+ as='int((nf+2)/2) * W / nf * 0.29' pd='2*int((nf+1)/2) * (W / nf + 0.29)' ps='2*int((nf+2)/2) * (W / nf + 0.29)'
+ nrd='0.29 / W ' nrs='0.29 / W ' sa=0 sb=0 sd=0 mult=1 m=1
XMP6 net19 VGP VDD VDD sky130_fd_pr__pfet_01v8_lvt L=8 W='0.55 * 7 ' nf=7 ad='int((nf+1)/2) * W / nf * 0.29'
+ as='int((nf+2)/2) * W / nf * 0.29' pd='2*int((nf+1)/2) * (W / nf + 0.29)' ps='2*int((nf+2)/2) * (W / nf + 0.29)'
+ nrd='0.29 / W ' nrs='0.29 / W ' sa=0 sb=0 sd=0 mult=1 m=1
XMN16 curr_n1 VGN net20 VSS sky130_fd_pr__nfet_01v8_lvt L=8 W='7 * 1 ' nf=1 ad='int((nf+1)/2) * W / nf * 0.29'
+ as='int((nf+2)/2) * W / nf * 0.29' pd='2*int((nf+1)/2) * (W / nf + 0.29)' ps='2*int((nf+2)/2) * (W / nf + 0.29)'
+ nrd='0.29 / W ' nrs='0.29 / W ' sa=0 sb=0 sd=0 mult=1 m=1
XMN17 net20 VGN VSS VSS sky130_fd_pr__nfet_01v8_lvt L=8 W='7 * 1 ' nf=1 ad='int((nf+1)/2) * W / nf * 0.29'
+ as='int((nf+2)/2) * W / nf * 0.29' pd='2*int((nf+1)/2) * (W / nf + 0.29)' ps='2*int((nf+2)/2) * (W / nf + 0.29)'
+ nrd='0.29 / W ' nrs='0.29 / W ' sa=0 sb=0 sd=0 mult=1 m=1
XM6 VGP net21 VGN VSS sky130_fd_pr__nfet_01v8 L=4 W='1 * 1 ' nf=1 ad='int((nf+1)/2) * W / nf * 0.29'
+ as='int((nf+2)/2) * W / nf * 0.29' pd='2*int((nf+1)/2) * (W / nf + 0.29)' ps='2*int((nf+2)/2) * (W / nf + 0.29)'
+ nrd='0.29 / W ' nrs='0.29 / W ' sa=0 sb=0 sd=0 mult=1 m=1
XM7 net21 Vrefgate VSS VSS sky130_fd_pr__nfet_01v8 L=4 W='1 * 1 ' nf=1 ad='int((nf+1)/2) * W / nf * 0.29'
+ as='int((nf+2)/2) * W / nf * 0.29' pd='2*int((nf+1)/2) * (W / nf + 0.29)' ps='2*int((nf+2)/2) * (W / nf + 0.29)'
+ nrd='0.29 / W ' nrs='0.29 / W ' sa=0 sb=0 sd=0 mult=1 m=1
XC1 VDD net21 VSS sky130_fd_pr__cap_var_lvt W=2 L=2 VM=1 m=1
XMN18 curr_n2 VGN net22 VSS sky130_fd_pr__nfet_01v8_lvt L=8 W='7 * 1 ' nf=1 ad='int((nf+1)/2) * W / nf * 0.29'
+ as='int((nf+2)/2) * W / nf * 0.29' pd='2*int((nf+1)/2) * (W / nf + 0.29)' ps='2*int((nf+2)/2) * (W / nf + 0.29)'
+ nrd='0.29 / W ' nrs='0.29 / W ' sa=0 sb=0 sd=0 mult=1 m=1
XMN19 net22 VGN VSS VSS sky130_fd_pr__nfet_01v8_lvt L=8 W='7 * 1 ' nf=1 ad='int((nf+1)/2) * W / nf * 0.29'
+ as='int((nf+2)/2) * W / nf * 0.29' pd='2*int((nf+1)/2) * (W / nf + 0.29)' ps='2*int((nf+2)/2) * (W / nf + 0.29)'
+ nrd='0.29 / W ' nrs='0.29 / W ' sa=0 sb=0 sd=0 mult=1 m=1
.ends


* expanding   symbol:  ldo_fc_n.sym # of pins=9
** sym_path: xschem/ldo_fc_n.sym
** sch_path: xschem/ldo_fc_n.sch
.subckt ldo_fc_n VDD inp inn bias1 bias2 bias3 outn VSS bias4
*.iopin VSS
*.iopin VDD
*.ipin inp
*.ipin inn
*.ipin bias1
*.opin outn
*.ipin bias2
*.ipin bias3
*.ipin bias4
XMN4 outn bias3 net1 VSS sky130_fd_pr__nfet_01v8_lvt L=4 W='1 * 9 ' nf=9 ad='int((nf+1)/2) * W / nf * 0.29'
+ as='int((nf+2)/2) * W / nf * 0.29' pd='2*int((nf+1)/2) * (W / nf + 0.29)' ps='2*int((nf+2)/2) * (W / nf + 0.29)'
+ nrd='0.29 / W ' nrs='0.29 / W ' sa=0 sb=0 sd=0 mult=12 m=12
XMN7 net1 net3 net8 VSS sky130_fd_pr__nfet_01v8_lvt L=4 W='1 * 3 ' nf=3 ad='int((nf+1)/2) * W / nf * 0.29'
+ as='int((nf+2)/2) * W / nf * 0.29' pd='2*int((nf+1)/2) * (W / nf + 0.29)' ps='2*int((nf+2)/2) * (W / nf + 0.29)'
+ nrd='0.29 / W ' nrs='0.29 / W ' sa=0 sb=0 sd=0 mult=12 m=12
XMN3 net3 bias3 net2 VSS sky130_fd_pr__nfet_01v8_lvt L=4 W='1 * 9 ' nf=9 ad='int((nf+1)/2) * W / nf * 0.29'
+ as='int((nf+2)/2) * W / nf * 0.29' pd='2*int((nf+1)/2) * (W / nf + 0.29)' ps='2*int((nf+2)/2) * (W / nf + 0.29)'
+ nrd='0.29 / W ' nrs='0.29 / W ' sa=0 sb=0 sd=0 mult=12 m=12
XMN6 net2 net3 net7 VSS sky130_fd_pr__nfet_01v8_lvt L=4 W='1 * 3 ' nf=3 ad='int((nf+1)/2) * W / nf * 0.29'
+ as='int((nf+2)/2) * W / nf * 0.29' pd='2*int((nf+1)/2) * (W / nf + 0.29)' ps='2*int((nf+2)/2) * (W / nf + 0.29)'
+ nrd='0.29 / W ' nrs='0.29 / W ' sa=0 sb=0 sd=0 mult=12 m=12
XMP4 outn bias2 net5 VDD sky130_fd_pr__pfet_01v8_lvt L=1 W='3 * 9 ' nf=9 ad='int((nf+1)/2) * W / nf * 0.29'
+ as='int((nf+2)/2) * W / nf * 0.29' pd='2*int((nf+1)/2) * (W / nf + 0.29)' ps='2*int((nf+2)/2) * (W / nf + 0.29)'
+ nrd='0.29 / W ' nrs='0.29 / W ' sa=0 sb=0 sd=0 mult=12 m=12
XMP2 net5 bias1 VDD VDD sky130_fd_pr__pfet_01v8_lvt L=8 W='1 * 3 ' nf=3 ad='int((nf+1)/2) * W / nf * 0.29'
+ as='int((nf+2)/2) * W / nf * 0.29' pd='2*int((nf+1)/2) * (W / nf + 0.29)' ps='2*int((nf+2)/2) * (W / nf + 0.29)'
+ nrd='0.29 / W ' nrs='0.29 / W ' sa=0 sb=0 sd=0 mult=19 m=19
XMP3 net3 bias2 net4 VDD sky130_fd_pr__pfet_01v8_lvt L=1 W='3 * 9 ' nf=9 ad='int((nf+1)/2) * W / nf * 0.29'
+ as='int((nf+2)/2) * W / nf * 0.29' pd='2*int((nf+1)/2) * (W / nf + 0.29)' ps='2*int((nf+2)/2) * (W / nf + 0.29)'
+ nrd='0.29 / W ' nrs='0.29 / W ' sa=0 sb=0 sd=0 mult=12 m=12
XMP1 net4 bias1 VDD VDD sky130_fd_pr__pfet_01v8_lvt L=8 W='1 * 3 ' nf=3 ad='int((nf+1)/2) * W / nf * 0.29'
+ as='int((nf+2)/2) * W / nf * 0.29' pd='2*int((nf+1)/2) * (W / nf + 0.29)' ps='2*int((nf+2)/2) * (W / nf + 0.29)'
+ nrd='0.29 / W ' nrs='0.29 / W ' sa=0 sb=0 sd=0 mult=19 m=19
XMN5 net6 bias4 net9 VSS sky130_fd_pr__nfet_01v8_lvt L=4 W='1 * 3 ' nf=3 ad='int((nf+1)/2) * W / nf * 0.29'
+ as='int((nf+2)/2) * W / nf * 0.29' pd='2*int((nf+1)/2) * (W / nf + 0.29)' ps='2*int((nf+2)/2) * (W / nf + 0.29)'
+ nrd='0.29 / W ' nrs='0.29 / W ' sa=0 sb=0 sd=0 mult=14 m=14
XMN1 net4 inn net6 VSS sky130_fd_pr__nfet_01v8_lvt L=0.25 W='7 * 5 ' nf=5 ad='int((nf+1)/2) * W / nf * 0.29'
+ as='int((nf+2)/2) * W / nf * 0.29' pd='2*int((nf+1)/2) * (W / nf + 0.29)' ps='2*int((nf+2)/2) * (W / nf + 0.29)'
+ nrd='0.29 / W ' nrs='0.29 / W ' sa=0 sb=0 sd=0 mult=1 m=1
XMN2 net5 inp net6 VSS sky130_fd_pr__nfet_01v8_lvt L=0.25 W='7 * 5 ' nf=5 ad='int((nf+1)/2) * W / nf * 0.29'
+ as='int((nf+2)/2) * W / nf * 0.29' pd='2*int((nf+1)/2) * (W / nf + 0.29)' ps='2*int((nf+2)/2) * (W / nf + 0.29)'
+ nrd='0.29 / W ' nrs='0.29 / W ' sa=0 sb=0 sd=0 mult=1 m=1
XMN9 net8 net3 net10 VSS sky130_fd_pr__nfet_01v8_lvt L=4 W='1 * 3 ' nf=3 ad='int((nf+1)/2) * W / nf * 0.29'
+ as='int((nf+2)/2) * W / nf * 0.29' pd='2*int((nf+1)/2) * (W / nf + 0.29)' ps='2*int((nf+2)/2) * (W / nf + 0.29)'
+ nrd='0.29 / W ' nrs='0.29 / W ' sa=0 sb=0 sd=0 mult=12 m=12
XMN10 net7 net3 net11 VSS sky130_fd_pr__nfet_01v8_lvt L=4 W='1 * 3 ' nf=3 ad='int((nf+1)/2) * W / nf * 0.29'
+ as='int((nf+2)/2) * W / nf * 0.29' pd='2*int((nf+1)/2) * (W / nf + 0.29)' ps='2*int((nf+2)/2) * (W / nf + 0.29)'
+ nrd='0.29 / W ' nrs='0.29 / W ' sa=0 sb=0 sd=0 mult=12 m=12
XMN11 net9 bias4 net12 VSS sky130_fd_pr__nfet_01v8_lvt L=4 W='1 * 3 ' nf=3 ad='int((nf+1)/2) * W / nf * 0.29'
+ as='int((nf+2)/2) * W / nf * 0.29' pd='2*int((nf+1)/2) * (W / nf + 0.29)' ps='2*int((nf+2)/2) * (W / nf + 0.29)'
+ nrd='0.29 / W ' nrs='0.29 / W ' sa=0 sb=0 sd=0 mult=14 m=14
XMN8 net10 net3 VSS VSS sky130_fd_pr__nfet_01v8_lvt L=4 W='1 * 3 ' nf=3 ad='int((nf+1)/2) * W / nf * 0.29'
+ as='int((nf+2)/2) * W / nf * 0.29' pd='2*int((nf+1)/2) * (W / nf + 0.29)' ps='2*int((nf+2)/2) * (W / nf + 0.29)'
+ nrd='0.29 / W ' nrs='0.29 / W ' sa=0 sb=0 sd=0 mult=12 m=12
XMN12 net11 net3 VSS VSS sky130_fd_pr__nfet_01v8_lvt L=4 W='1 * 3 ' nf=3 ad='int((nf+1)/2) * W / nf * 0.29'
+ as='int((nf+2)/2) * W / nf * 0.29' pd='2*int((nf+1)/2) * (W / nf + 0.29)' ps='2*int((nf+2)/2) * (W / nf + 0.29)'
+ nrd='0.29 / W ' nrs='0.29 / W ' sa=0 sb=0 sd=0 mult=12 m=12
XMN13 net12 bias4 VSS VSS sky130_fd_pr__nfet_01v8_lvt L=4 W='1 * 3 ' nf=3 ad='int((nf+1)/2) * W / nf * 0.29'
+ as='int((nf+2)/2) * W / nf * 0.29' pd='2*int((nf+1)/2) * (W / nf + 0.29)' ps='2*int((nf+2)/2) * (W / nf + 0.29)'
+ nrd='0.29 / W ' nrs='0.29 / W ' sa=0 sb=0 sd=0 mult=14 m=14
.ends

.GLOBAL GND
.end
